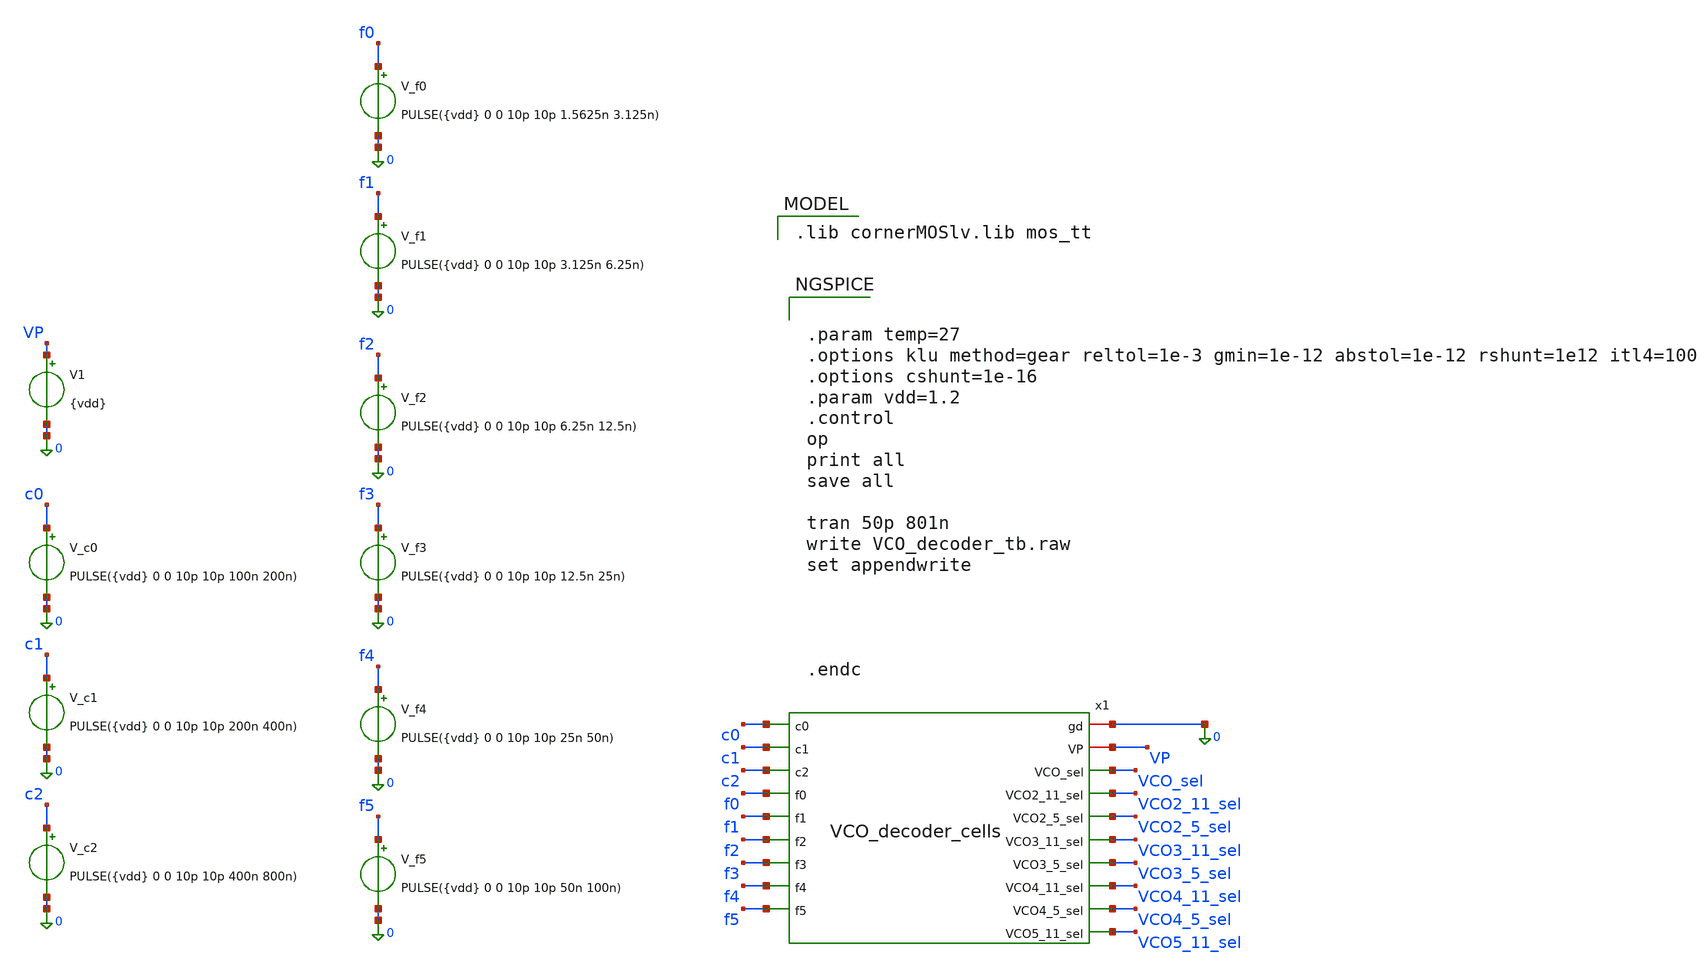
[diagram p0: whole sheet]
** sch_path: PLL0663-main/testbenches/tran/xschem/divider/VCO_decoder_tb.sch
**.subckt VCO_decoder_tb
V1 VP 0 {vdd}
V_c0 c0 0 PULSE({vdd} 0 0 10p 10p 100n 200n)
V_f1 f1 0 PULSE({vdd} 0 0 10p 10p 3.125n 6.25n)
V_c1 c1 0 PULSE({vdd} 0 0 10p 10p 200n 400n)
V_c2 c2 0 PULSE({vdd} 0 0 10p 10p 400n 800n)
V_f0 f0 0 PULSE({vdd} 0 0 10p 10p 1.5625n 3.125n)
x1 0 VP c0 c1 c2 f0 f1 f2 f3 f4 f5 VCO_sel VCO2_11_sel VCO2_5_sel VCO3_11_sel VCO3_5_sel VCO4_11_sel
+ VCO4_5_sel VCO5_11_sel VCO_decoder_cells
V_f3 f3 0 PULSE({vdd} 0 0 10p 10p 12.5n 25n)
V_f2 f2 0 PULSE({vdd} 0 0 10p 10p 6.25n 12.5n)
V_f5 f5 0 PULSE({vdd} 0 0 10p 10p 50n 100n)
V_f4 f4 0 PULSE({vdd} 0 0 10p 10p 25n 50n)
**** begin user architecture code
 .lib cornerMOSlv.lib mos_tt



.param temp=27
.options klu method=gear reltol=1e-3 gmin=1e-12 abstol=1e-12 rshunt=1e12 itl4=100
.options cshunt=1e-16
.param vdd=1.2
.control
op
print all
save all

tran 50p 801n
write VCO_decoder_tb.raw
set appendwrite




.endc


**** end user architecture code
**.ends
.end
